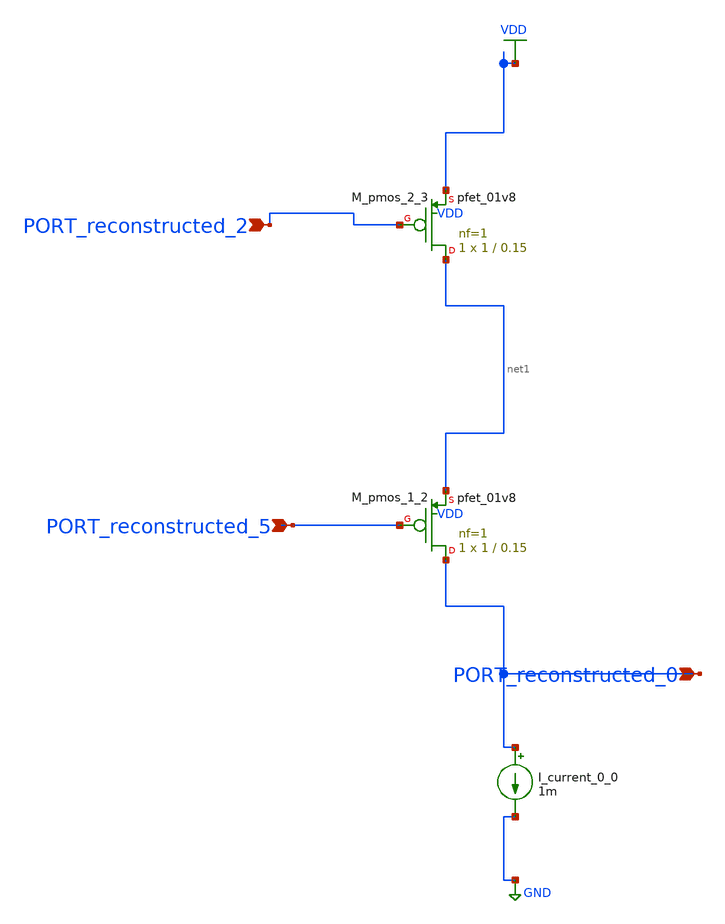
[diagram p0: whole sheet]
** sch_path: schematics/AMSNet/634.sch
**.subckt 634 PORT_reconstructed_5 PORT_reconstructed_2 PORT_reconstructed_0
*.ipin PORT_reconstructed_5
*.ipin PORT_reconstructed_2
*.ipin PORT_reconstructed_0
I_current_0_0 PORT_reconstructed_0 GND 1m
XM_pmos_1_2 PORT_reconstructed_0 PORT_reconstructed_5 net1 VDD sky130_fd_pr__pfet_01v8 L=0.15 W=1 nf=1
+ ad='int((1 + 1)/2) * 1 / 1 * 0.29' as='int((1 + 2)/2) * 1 / 1 * 0.29' pd='2*int((1 + 1)/2) * (1 / 1 + 0.29)'
+ ps='2*int((1 + 2)/2) * (1 / 1 + 0.29)' nrd='0.29 / 1 ' nrs='0.29 / 1 ' sa=0 sb=0 sd=0 mult=1 m=1
XM_pmos_2_3 net1 PORT_reconstructed_2 VDD VDD sky130_fd_pr__pfet_01v8 L=0.15 W=1 nf=1 ad='int((1 + 1)/2) * 1 / 1 * 0.29'
+ as='int((1 + 2)/2) * 1 / 1 * 0.29' pd='2*int((1 + 1)/2) * (1 / 1 + 0.29)' ps='2*int((1 + 2)/2) * (1 / 1 + 0.29)'
+ nrd='0.29 / 1 ' nrs='0.29 / 1 ' sa=0 sb=0 sd=0 mult=1 m=1
**.ends
.GLOBAL GND
.GLOBAL VDD
.end
